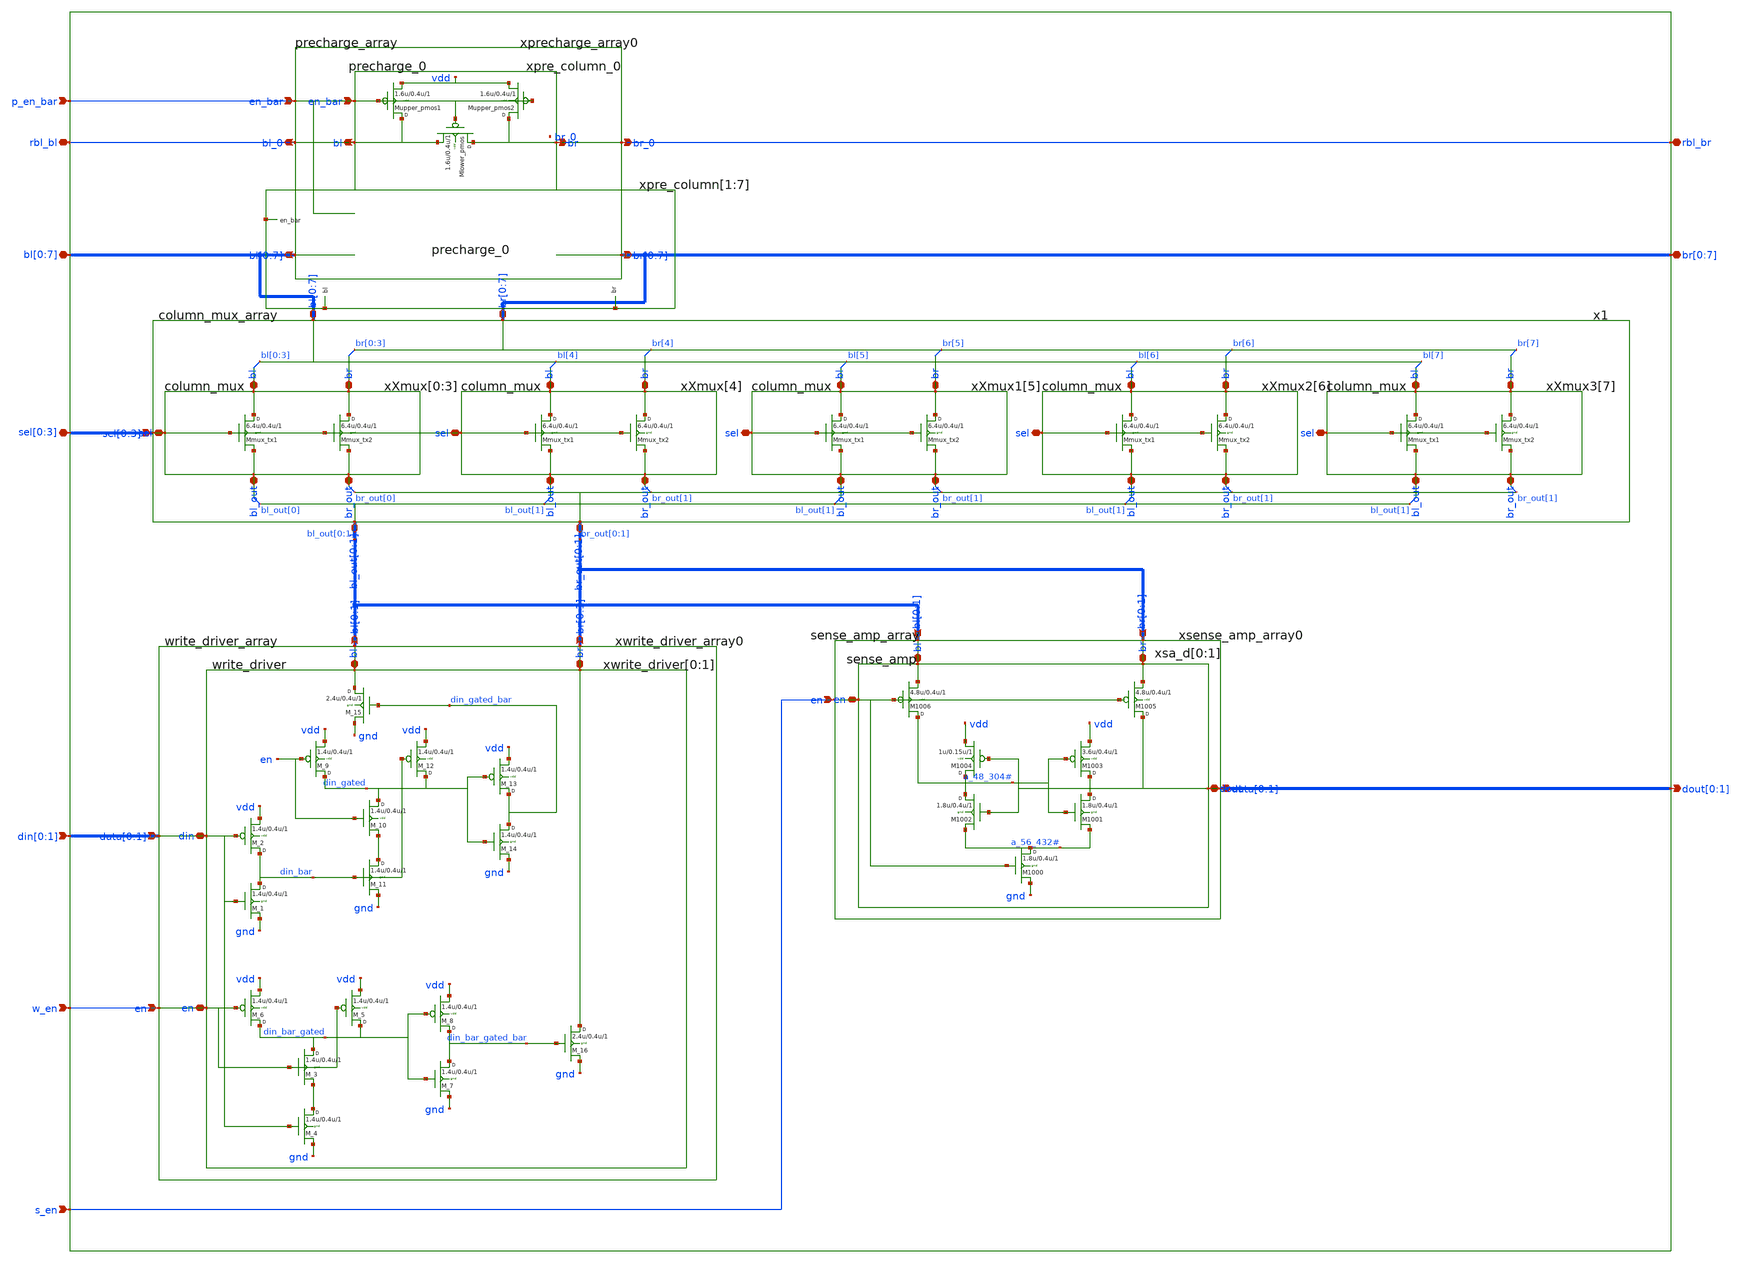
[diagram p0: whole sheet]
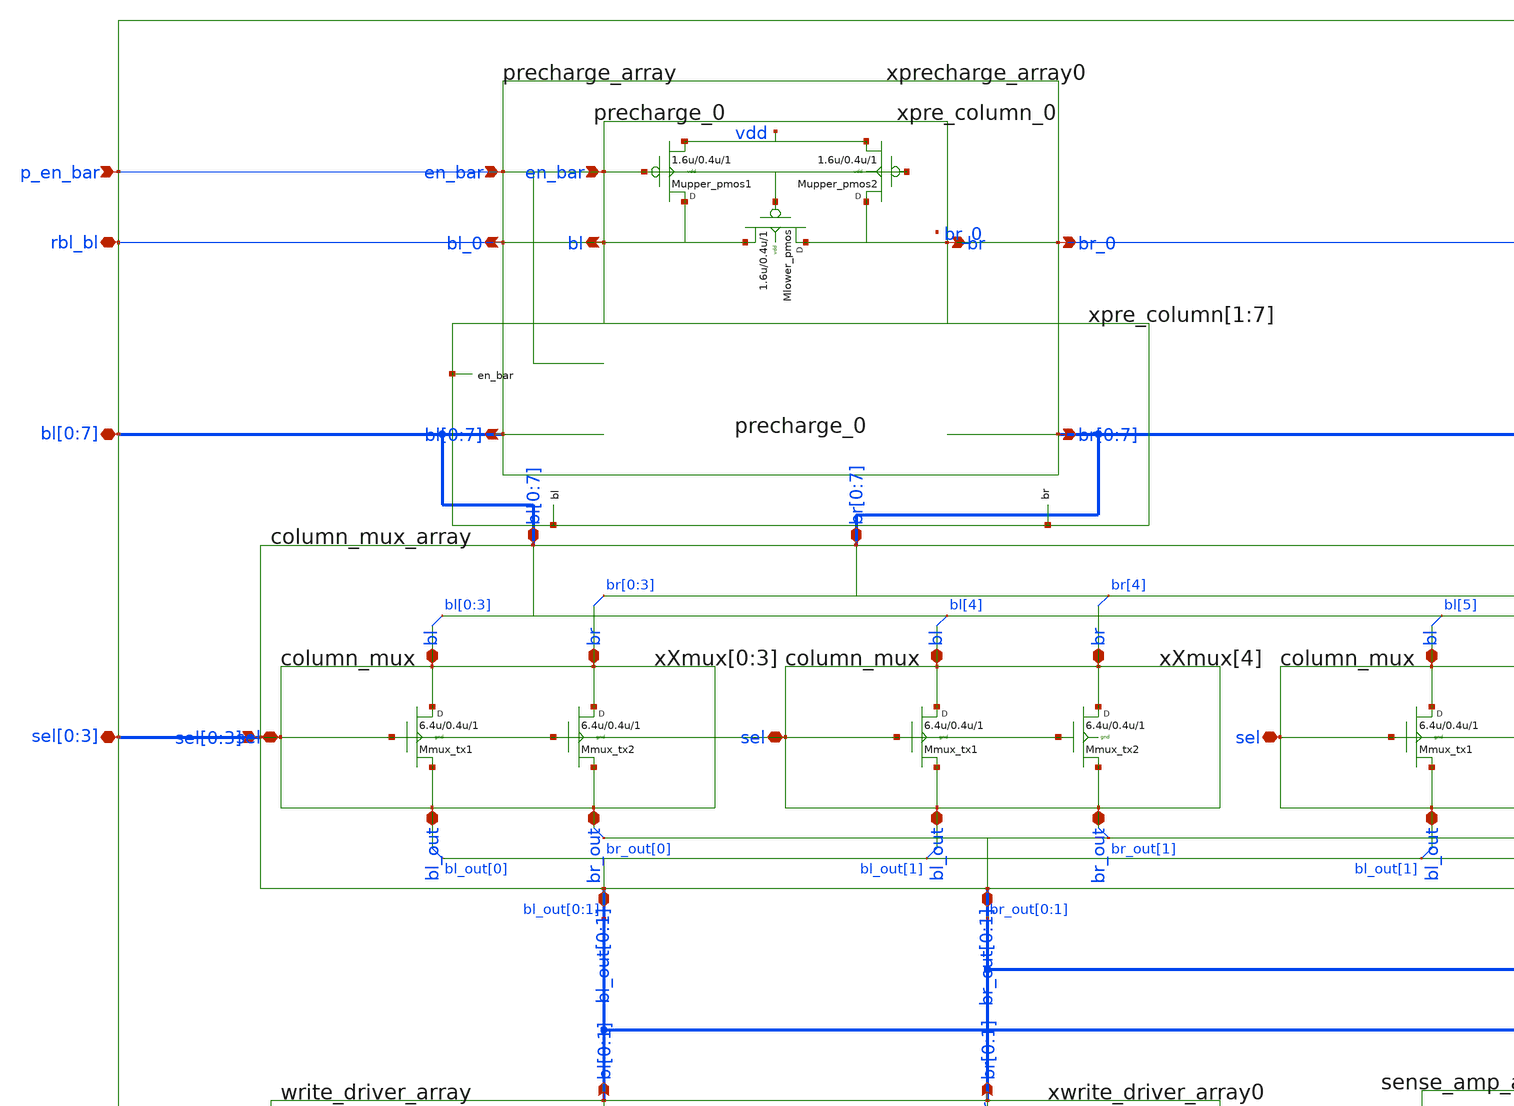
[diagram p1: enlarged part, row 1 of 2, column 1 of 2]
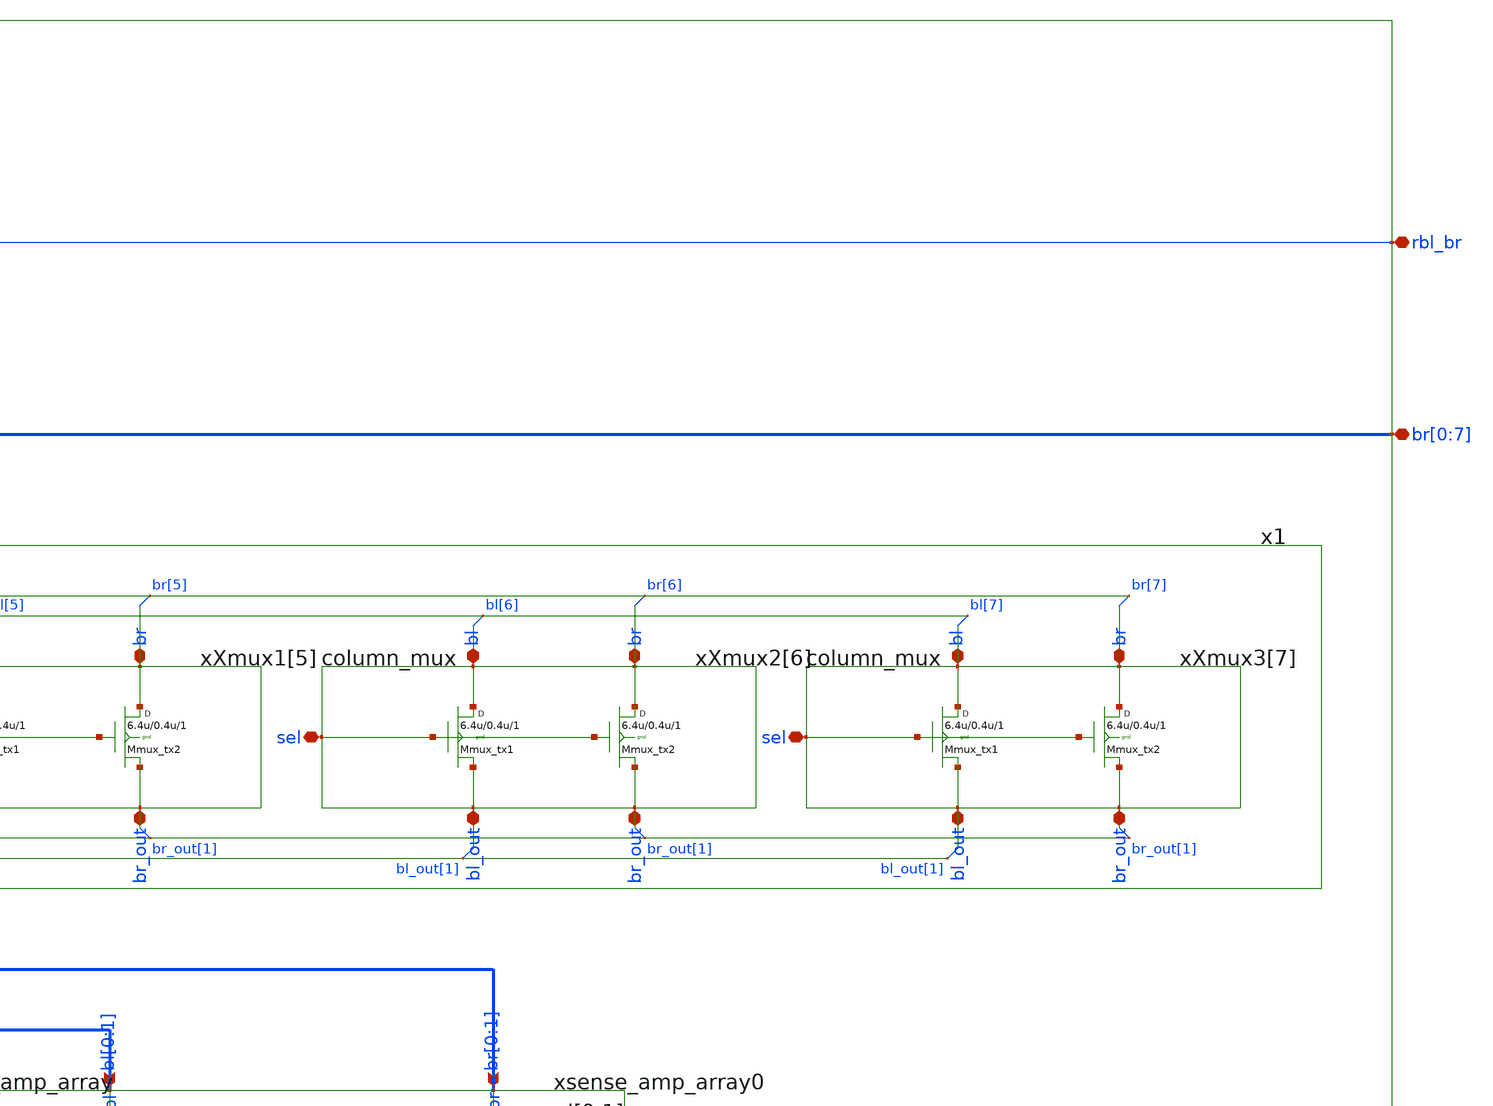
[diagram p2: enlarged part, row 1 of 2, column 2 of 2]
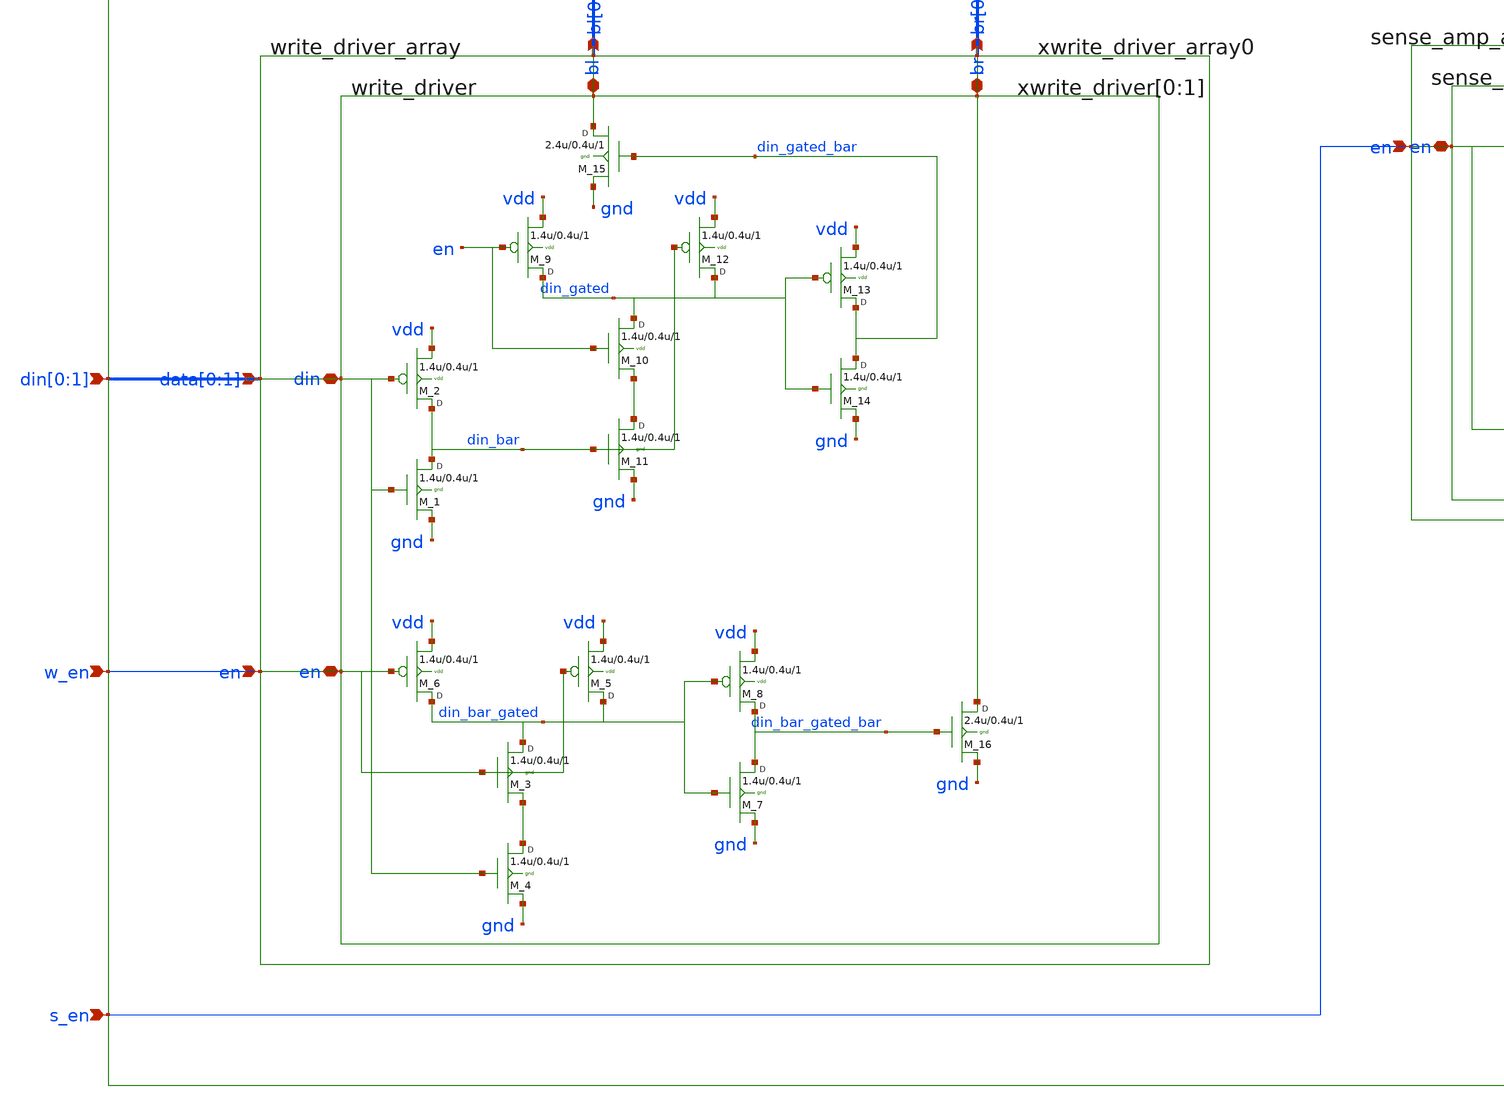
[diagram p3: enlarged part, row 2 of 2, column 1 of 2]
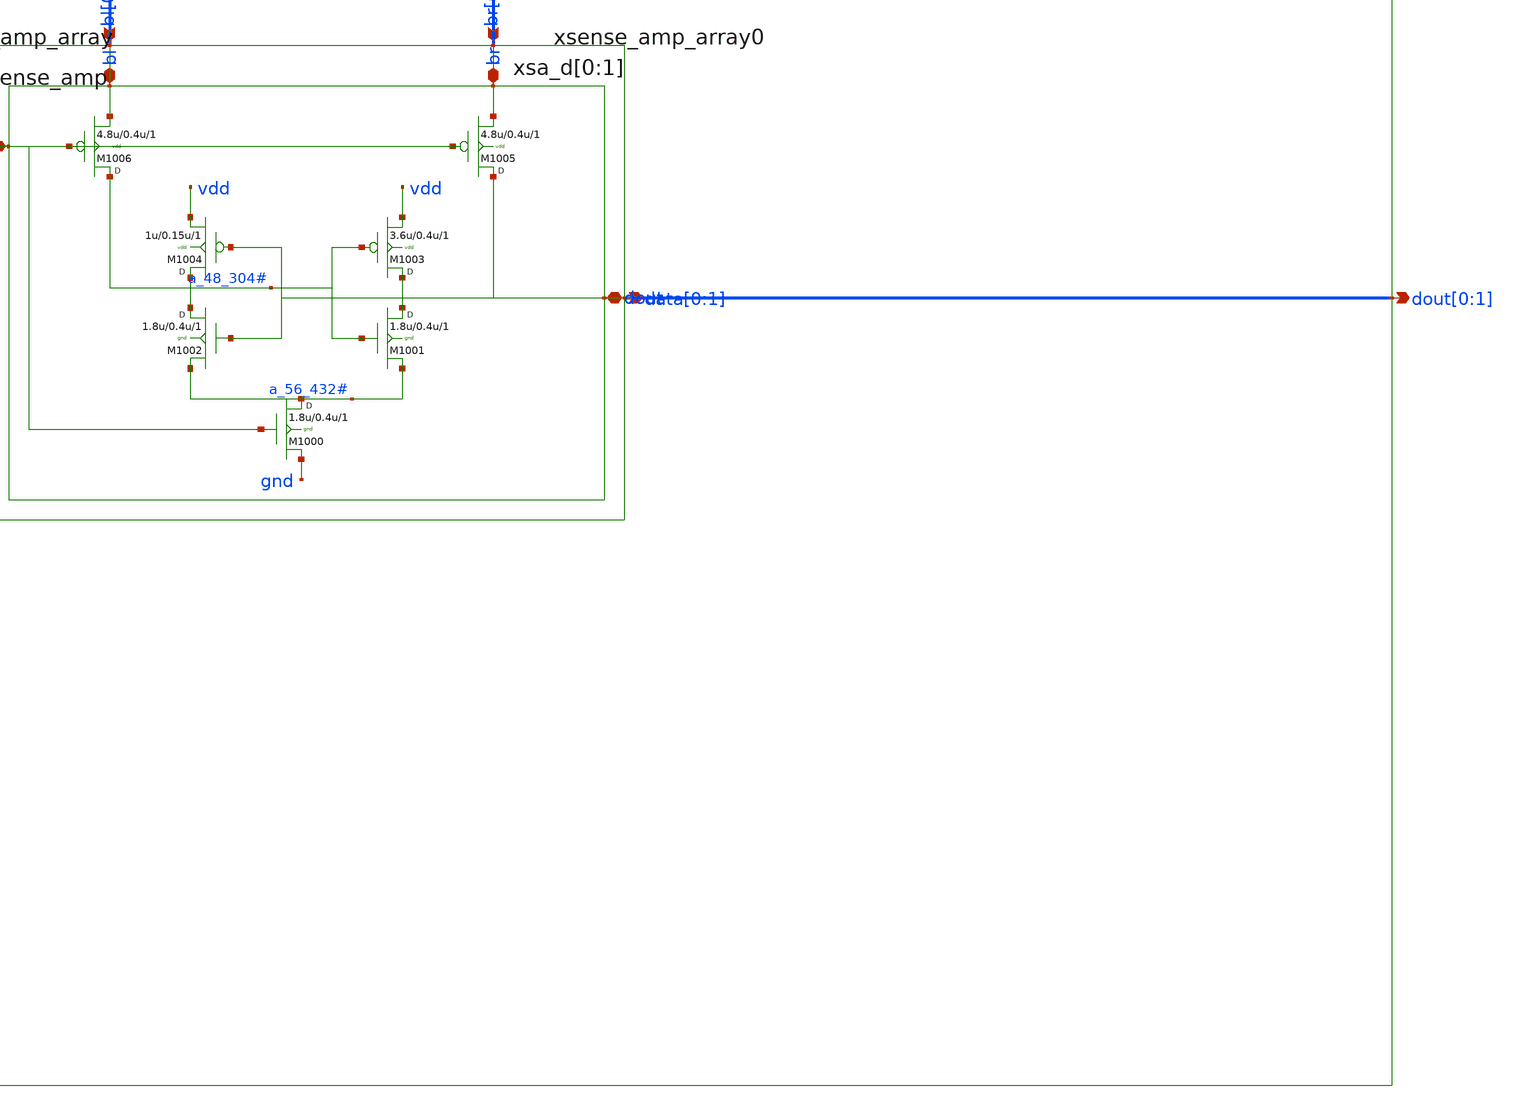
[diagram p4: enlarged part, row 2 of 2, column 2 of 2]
** sch_path: sram_2_64_scn4m/port_data.sch
**.subckt port_data rbl_bl rbl_br bl[0],bl[1],bl[2],bl[3],bl[4],bl[5],bl[6],bl[7]
*+ br[0],br[1],br[2],br[3],br[4],br[5],br[6],br[7] dout[0],dout[1] din[0],din[1] s_en p_en_bar w_en sel[0],sel[1],sel[2],sel[3]
*.iopin rbl_bl
*.iopin rbl_br
*.iopin bl[0],bl[1],bl[2],bl[3],bl[4],bl[5],bl[6],bl[7]
*.iopin br[0],br[1],br[2],br[3],br[4],br[5],br[6],br[7]
*.opin dout[0],dout[1]
*.ipin din[0],din[1]
*.ipin s_en
*.ipin p_en_bar
*.ipin w_en
*.iopin sel[0],sel[1],sel[2],sel[3]
xprecharge_array0 rbl_bl rbl_br bl[0] bl[1] bl[2] bl[3] bl[4] bl[5] bl[6] bl[7] br[0] br[1] br[2]
+ br[3] br[4] br[5] br[6] br[7] p_en_bar vdd precharge_array
xwrite_driver_array0 din[0] din[1] bl_out[0] bl_out[1] br_out[0] br_out[1] w_en vdd gnd
+ write_driver_array
xsense_amp_array0 dout[0] dout[1] bl_out[0] bl_out[1] br_out[0] br_out[1] s_en vdd gnd
+ sense_amp_array
x1 bl[0] bl[1] bl[2] bl[3] bl[4] bl[5] bl[6] bl[7] br[0] br[1] br[2] br[3] br[4] br[5] br[6] br[7]
+ sel[0] sel[1] sel[2] sel[3] br_out[0] br_out[1] bl_out[0] bl_out[1] vdd gnd column_mux_array
**.ends
.end
